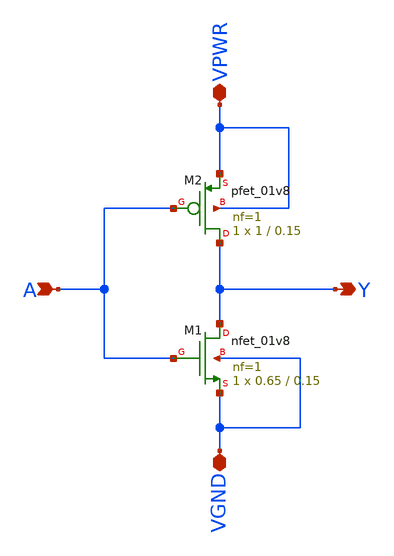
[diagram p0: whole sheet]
** sch_path: inverter/inv.sch
**.subckt inv VPWR VGND A Y
*.iopin VPWR
*.iopin VGND
*.ipin A
*.opin Y
XM1 Y A VGND VGND sky130_fd_pr__nfet_01v8 L=0.15 W=0.65 nf=1 ad='int((1 + 1)/2) * 0.65 / 1 * 0.29' as='int((1 + 2)/2) * 0.65 / 1 * 0.29'
+ pd='2*int((1 + 1)/2) * (0.65 / 1 + 0.29)' ps='2*int((1 + 2)/2) * (0.65 / 1 + 0.29)' nrd='0.29 / 0.65 '
+ nrs='0.29 / 0.65 ' sa=0 sb=0 sd=0 mult=1 m=1
XM2 Y A VPWR VPWR sky130_fd_pr__pfet_01v8 L=0.15 W=1 nf=1 ad='int((1 + 1)/2) * 1 / 1 * 0.29' as='int((1 + 2)/2) * 1 / 1 * 0.29'
+ pd='2*int((1 + 1)/2) * (1 / 1 + 0.29)' ps='2*int((1 + 2)/2) * (1 / 1 + 0.29)' nrd='0.29 / 1 ' nrs='0.29 / 1 '
+ sa=0 sb=0 sd=0 mult=1 m=1
**.ends
.end
